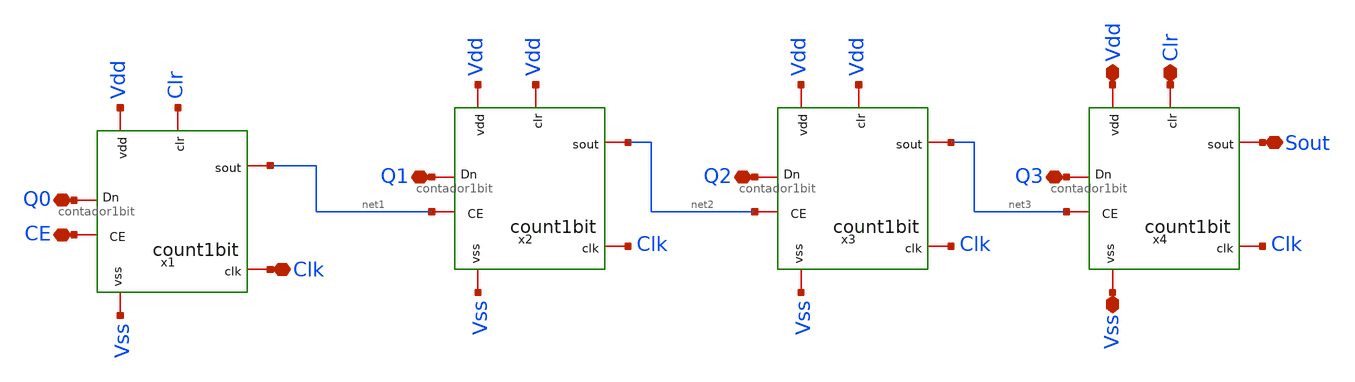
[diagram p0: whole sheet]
** sch_path: design/blocks/circuito_completo/circuito_completo.sch
**.subckt circuito_completo CE Clk Vss Clr Vdd Q0 Q1 Q2 Sout Q3
*.iopin CE
*.iopin Clk
*.iopin Vss
*.iopin Clr
*.iopin Vdd
*.iopin Q0
*.iopin Q1
*.iopin Q2
*.iopin Sout
*.iopin Q3
x1 Clr Q0 CE Clk Vdd Vss net1 contador1bit
x2 Vdd Q1 net1 Clk Vdd Vss net2 contador1bit
x3 Vdd Q2 net2 Clk Vdd Vss net3 contador1bit
x4 Clr Q3 net3 Clk Vdd Vss Sout contador1bit
**.ends
.end
